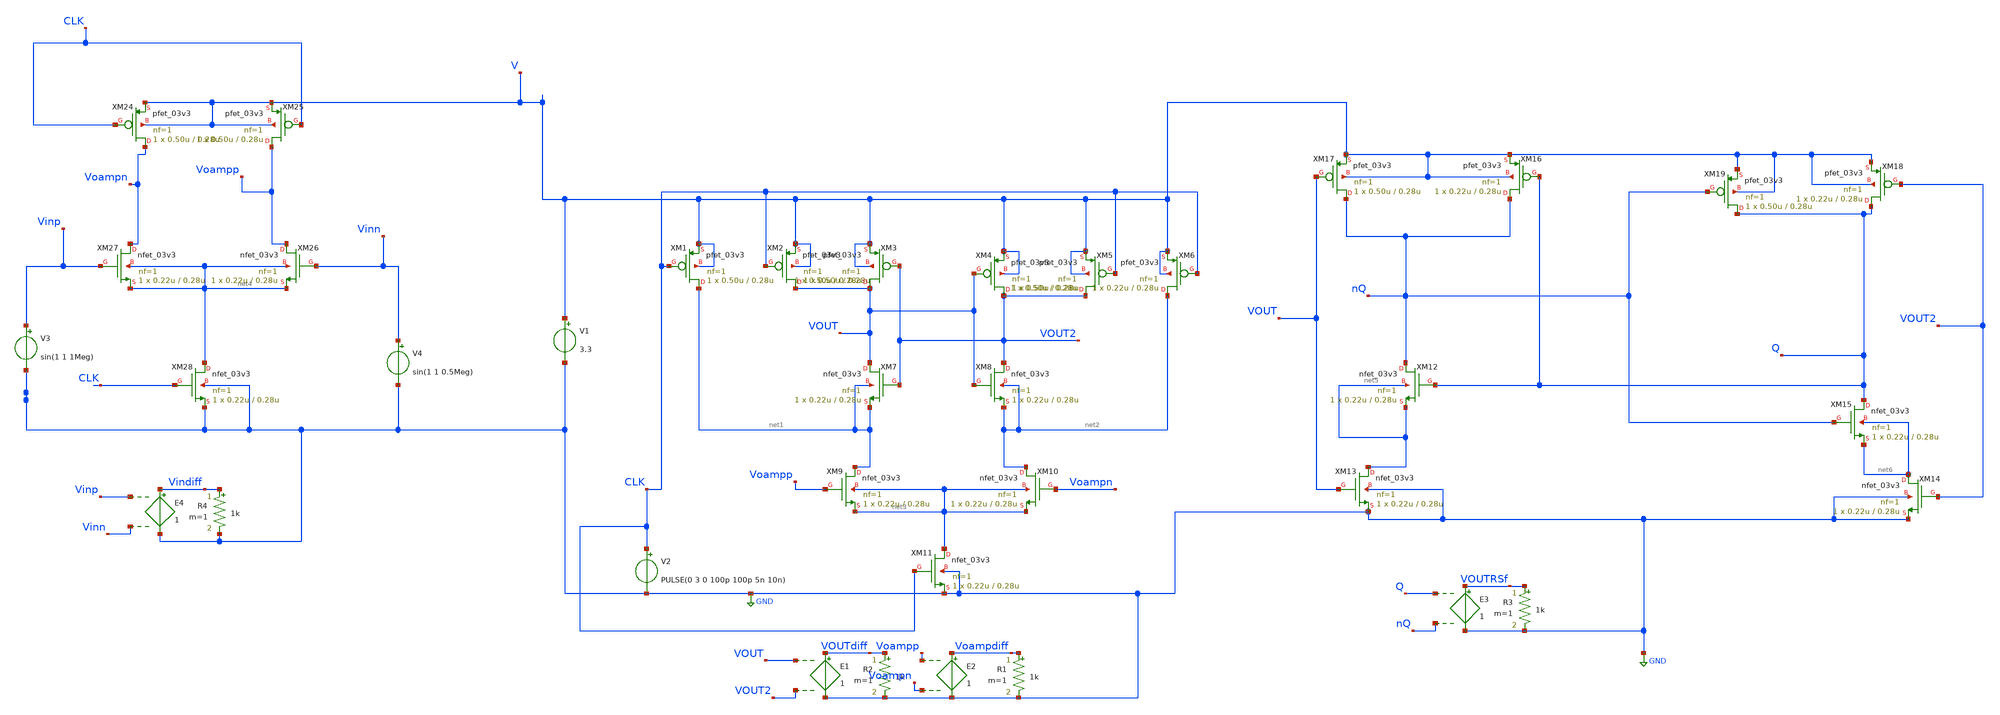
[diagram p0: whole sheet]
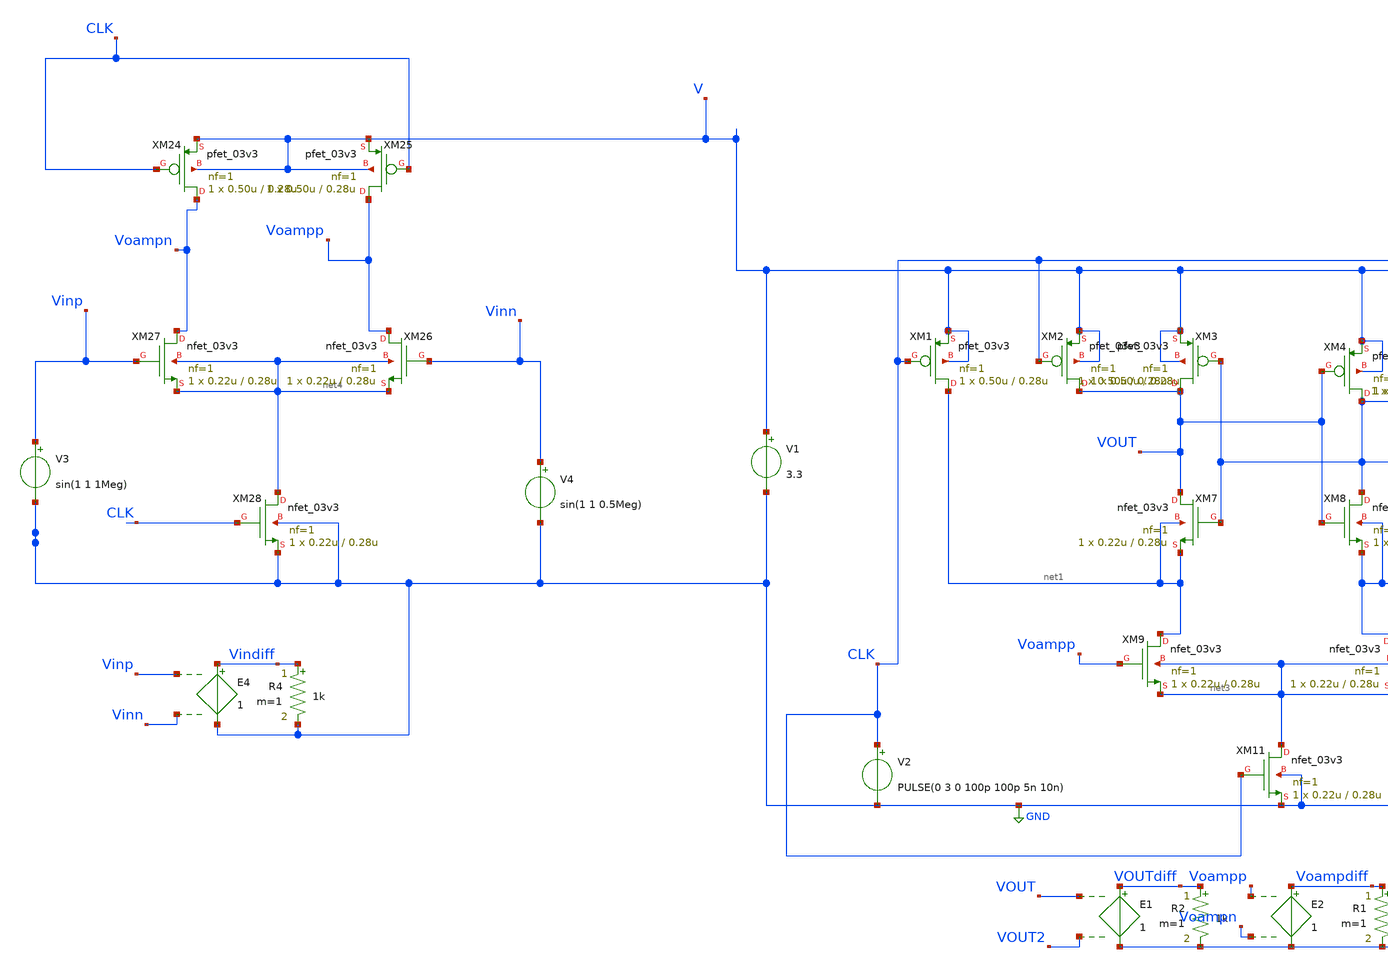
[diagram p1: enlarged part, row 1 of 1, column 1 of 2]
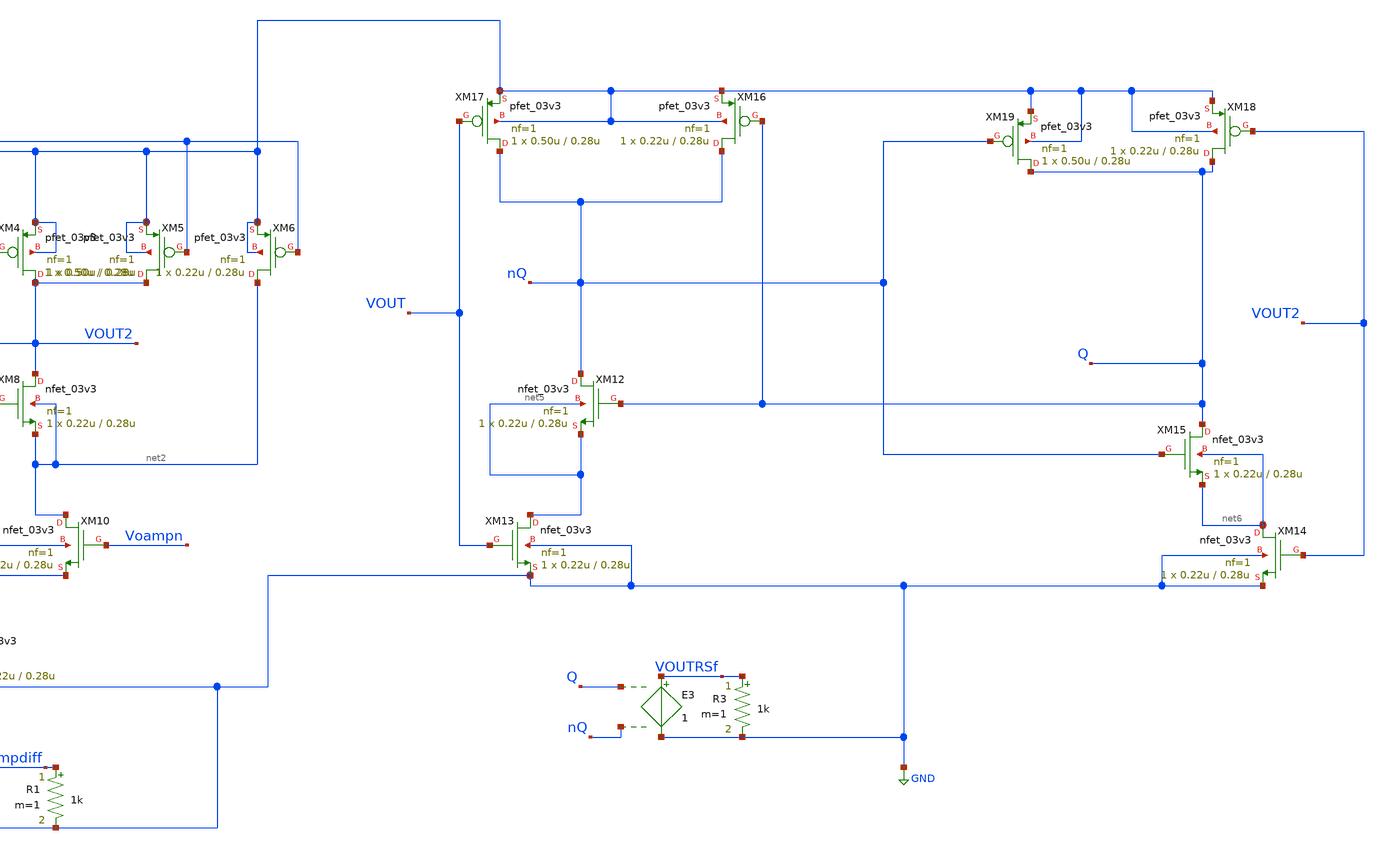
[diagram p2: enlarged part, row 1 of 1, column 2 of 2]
** sch_path: Comparador_pream_latch.sch
**.subckt Comparador_pream_latch
XM1 net1 CLK V V pfet_03v3 L=0.28u W=0.50u nf=1 ad='int((nf+1)/2) * W/nf * 0.18u' as='int((nf+2)/2) * W/nf * 0.18u'
+ pd='2*int((nf+1)/2) * (W/nf + 0.18u)' ps='2*int((nf+2)/2) * (W/nf + 0.18u)' nrd='0.18u / W' nrs='0.18u / W'
+ sa=0 sb=0 sd=0 m=1
XM2 VOUT CLK V V pfet_03v3 L=0.28u W=0.50u nf=1 ad='int((nf+1)/2) * W/nf * 0.18u' as='int((nf+2)/2) * W/nf * 0.18u'
+ pd='2*int((nf+1)/2) * (W/nf + 0.18u)' ps='2*int((nf+2)/2) * (W/nf + 0.18u)' nrd='0.18u / W' nrs='0.18u / W'
+ sa=0 sb=0 sd=0 m=1
XM3 VOUT VOUT2 V V pfet_03v3 L=0.28u W=0.50u nf=1 ad='int((nf+1)/2) * W/nf * 0.18u' as='int((nf+2)/2) * W/nf * 0.18u'
+ pd='2*int((nf+1)/2) * (W/nf + 0.18u)' ps='2*int((nf+2)/2) * (W/nf + 0.18u)' nrd='0.18u / W' nrs='0.18u / W'
+ sa=0 sb=0 sd=0 m=1
XM4 VOUT2 VOUT V V pfet_03v3 L=0.28u W=0.50u nf=1 ad='int((nf+1)/2) * W/nf * 0.18u' as='int((nf+2)/2) * W/nf * 0.18u'
+ pd='2*int((nf+1)/2) * (W/nf + 0.18u)' ps='2*int((nf+2)/2) * (W/nf + 0.18u)' nrd='0.18u / W' nrs='0.18u / W'
+ sa=0 sb=0 sd=0 m=1
XM5 VOUT2 CLK V V pfet_03v3 L=0.28u W=0.50u nf=1 ad='int((nf+1)/2) * W/nf * 0.18u' as='int((nf+2)/2) * W/nf * 0.18u'
+ pd='2*int((nf+1)/2) * (W/nf + 0.18u)' ps='2*int((nf+2)/2) * (W/nf + 0.18u)' nrd='0.18u / W' nrs='0.18u / W'
+ sa=0 sb=0 sd=0 m=1
XM6 net2 CLK V V pfet_03v3 L=0.28u W=0.22u nf=1 ad='int((nf+1)/2) * W/nf * 0.18u' as='int((nf+2)/2) * W/nf * 0.18u'
+ pd='2*int((nf+1)/2) * (W/nf + 0.18u)' ps='2*int((nf+2)/2) * (W/nf + 0.18u)' nrd='0.18u / W' nrs='0.18u / W'
+ sa=0 sb=0 sd=0 m=1
XM7 VOUT VOUT2 net1 net1 nfet_03v3 L=0.28u W=0.22u nf=1 ad='int((nf+1)/2) * W/nf * 0.18u' as='int((nf+2)/2) * W/nf * 0.18u'
+ pd='2*int((nf+1)/2) * (W/nf + 0.18u)' ps='2*int((nf+2)/2) * (W/nf + 0.18u)' nrd='0.18u / W' nrs='0.18u / W'
+ sa=0 sb=0 sd=0 m=1
XM8 VOUT2 VOUT net2 net2 nfet_03v3 L=0.28u W=0.22u nf=1 ad='int((nf+1)/2) * W/nf * 0.18u' as='int((nf+2)/2) * W/nf * 0.18u'
+ pd='2*int((nf+1)/2) * (W/nf + 0.18u)' ps='2*int((nf+2)/2) * (W/nf + 0.18u)' nrd='0.18u / W' nrs='0.18u / W'
+ sa=0 sb=0 sd=0 m=1
XM9 net1 Voampp net3 net3 nfet_03v3 L=0.28u W=0.22u nf=1 ad='int((nf+1)/2) * W/nf * 0.18u' as='int((nf+2)/2) * W/nf * 0.18u'
+ pd='2*int((nf+1)/2) * (W/nf + 0.18u)' ps='2*int((nf+2)/2) * (W/nf + 0.18u)' nrd='0.18u / W' nrs='0.18u / W'
+ sa=0 sb=0 sd=0 m=1
XM10 net2 Voampn net3 net3 nfet_03v3 L=0.28u W=0.22u nf=1 ad='int((nf+1)/2) * W/nf * 0.18u' as='int((nf+2)/2) * W/nf * 0.18u'
+ pd='2*int((nf+1)/2) * (W/nf + 0.18u)' ps='2*int((nf+2)/2) * (W/nf + 0.18u)' nrd='0.18u / W' nrs='0.18u / W'
+ sa=0 sb=0 sd=0 m=1
XM11 net3 CLK GND GND nfet_03v3 L=0.28u W=0.22u nf=1 ad='int((nf+1)/2) * W/nf * 0.18u' as='int((nf+2)/2) * W/nf * 0.18u'
+ pd='2*int((nf+1)/2) * (W/nf + 0.18u)' ps='2*int((nf+2)/2) * (W/nf + 0.18u)' nrd='0.18u / W' nrs='0.18u / W'
+ sa=0 sb=0 sd=0 m=1
V1 V GND 3.3
V2 CLK GND PULSE(0 3 0 100p 100p 5n 10n)
R2 VOUTdiff GND 1k m=1
E1 VOUTdiff GND VOUT VOUT2 1
R1 Voampdiff GND 1k m=1
E2 Voampdiff GND Voampp Voampn 1
XM12 nQ Q net5 net5 nfet_03v3 L=0.28u W=0.22u nf=1 ad='int((nf+1)/2) * W/nf * 0.18u' as='int((nf+2)/2) * W/nf * 0.18u'
+ pd='2*int((nf+1)/2) * (W/nf + 0.18u)' ps='2*int((nf+2)/2) * (W/nf + 0.18u)' nrd='0.18u / W' nrs='0.18u / W'
+ sa=0 sb=0 sd=0 m=1
XM13 net5 VOUT GND GND nfet_03v3 L=0.28u W=0.22u nf=1 ad='int((nf+1)/2) * W/nf * 0.18u' as='int((nf+2)/2) * W/nf * 0.18u'
+ pd='2*int((nf+1)/2) * (W/nf + 0.18u)' ps='2*int((nf+2)/2) * (W/nf + 0.18u)' nrd='0.18u / W' nrs='0.18u / W'
+ sa=0 sb=0 sd=0 m=1
XM14 net6 VOUT2 GND GND nfet_03v3 L=0.28u W=0.22u nf=1 ad='int((nf+1)/2) * W/nf * 0.18u' as='int((nf+2)/2) * W/nf * 0.18u'
+ pd='2*int((nf+1)/2) * (W/nf + 0.18u)' ps='2*int((nf+2)/2) * (W/nf + 0.18u)' nrd='0.18u / W' nrs='0.18u / W'
+ sa=0 sb=0 sd=0 m=1
XM15 Q nQ net6 net6 nfet_03v3 L=0.28u W=0.22u nf=1 ad='int((nf+1)/2) * W/nf * 0.18u' as='int((nf+2)/2) * W/nf * 0.18u'
+ pd='2*int((nf+1)/2) * (W/nf + 0.18u)' ps='2*int((nf+2)/2) * (W/nf + 0.18u)' nrd='0.18u / W' nrs='0.18u / W'
+ sa=0 sb=0 sd=0 m=1
XM16 nQ Q V V pfet_03v3 L=0.28u W=0.22u nf=1 ad='int((nf+1)/2) * W/nf * 0.18u' as='int((nf+2)/2) * W/nf * 0.18u'
+ pd='2*int((nf+1)/2) * (W/nf + 0.18u)' ps='2*int((nf+2)/2) * (W/nf + 0.18u)' nrd='0.18u / W' nrs='0.18u / W'
+ sa=0 sb=0 sd=0 m=1
XM17 nQ VOUT V V pfet_03v3 L=0.28u W=0.50u nf=1 ad='int((nf+1)/2) * W/nf * 0.18u' as='int((nf+2)/2) * W/nf * 0.18u'
+ pd='2*int((nf+1)/2) * (W/nf + 0.18u)' ps='2*int((nf+2)/2) * (W/nf + 0.18u)' nrd='0.18u / W' nrs='0.18u / W'
+ sa=0 sb=0 sd=0 m=1
XM18 Q VOUT2 V V pfet_03v3 L=0.28u W=0.22u nf=1 ad='int((nf+1)/2) * W/nf * 0.18u' as='int((nf+2)/2) * W/nf * 0.18u'
+ pd='2*int((nf+1)/2) * (W/nf + 0.18u)' ps='2*int((nf+2)/2) * (W/nf + 0.18u)' nrd='0.18u / W' nrs='0.18u / W'
+ sa=0 sb=0 sd=0 m=1
XM19 Q nQ V V pfet_03v3 L=0.28u W=0.50u nf=1 ad='int((nf+1)/2) * W/nf * 0.18u' as='int((nf+2)/2) * W/nf * 0.18u'
+ pd='2*int((nf+1)/2) * (W/nf + 0.18u)' ps='2*int((nf+2)/2) * (W/nf + 0.18u)' nrd='0.18u / W' nrs='0.18u / W'
+ sa=0 sb=0 sd=0 m=1
R3 VOUTRSf GND 1k m=1
E3 VOUTRSf GND Q nQ 1
XM26 Voampp Vinn net4 net4 nfet_03v3 L=0.28u W=0.22u nf=1 ad='int((nf+1)/2) * W/nf * 0.18u' as='int((nf+2)/2) * W/nf * 0.18u'
+ pd='2*int((nf+1)/2) * (W/nf + 0.18u)' ps='2*int((nf+2)/2) * (W/nf + 0.18u)' nrd='0.18u / W' nrs='0.18u / W'
+ sa=0 sb=0 sd=0 m=1
XM27 Voampn Vinp net4 net4 nfet_03v3 L=0.28u W=0.22u nf=1 ad='int((nf+1)/2) * W/nf * 0.18u' as='int((nf+2)/2) * W/nf * 0.18u'
+ pd='2*int((nf+1)/2) * (W/nf + 0.18u)' ps='2*int((nf+2)/2) * (W/nf + 0.18u)' nrd='0.18u / W' nrs='0.18u / W'
+ sa=0 sb=0 sd=0 m=1
V3 Vinp GND sin(1 1 1Meg)
V4 Vinn GND sin(1 1 0.5Meg)
R4 Vindiff GND 1k m=1
E4 Vindiff GND Vinp Vinn 1
XM28 net4 CLK GND GND nfet_03v3 L=0.28u W=0.22u nf=1 ad='int((nf+1)/2) * W/nf * 0.18u' as='int((nf+2)/2) * W/nf * 0.18u'
+ pd='2*int((nf+1)/2) * (W/nf + 0.18u)' ps='2*int((nf+2)/2) * (W/nf + 0.18u)' nrd='0.18u / W' nrs='0.18u / W'
+ sa=0 sb=0 sd=0 m=1
XM24 Voampn CLK V V pfet_03v3 L=0.28u W=0.50u nf=1 ad='int((nf+1)/2) * W/nf * 0.18u' as='int((nf+2)/2) * W/nf * 0.18u'
+ pd='2*int((nf+1)/2) * (W/nf + 0.18u)' ps='2*int((nf+2)/2) * (W/nf + 0.18u)' nrd='0.18u / W' nrs='0.18u / W'
+ sa=0 sb=0 sd=0 m=1
XM25 Voampp CLK V V pfet_03v3 L=0.28u W=0.50u nf=1 ad='int((nf+1)/2) * W/nf * 0.18u' as='int((nf+2)/2) * W/nf * 0.18u'
+ pd='2*int((nf+1)/2) * (W/nf + 0.18u)' ps='2*int((nf+2)/2) * (W/nf + 0.18u)' nrd='0.18u / W' nrs='0.18u / W'
+ sa=0 sb=0 sd=0 m=1
**** begin user architecture code


.control
save all
tran 500p 10u
plot VOUTrsf Vindiff
plot VOUTdiff Vindiff
plot  Vindiff Voampdiff
plot VOUTdiff VOUTrsf
plot VOUT VOUT2
.endc


.include /foss/pdks/gf180mcuC/libs.tech/ngspice/design.ngspice
.lib /foss/pdks/gf180mcuC/libs.tech/ngspice/sm141064.ngspice typical

**** end user architecture code
**.ends
.GLOBAL GND
.end
